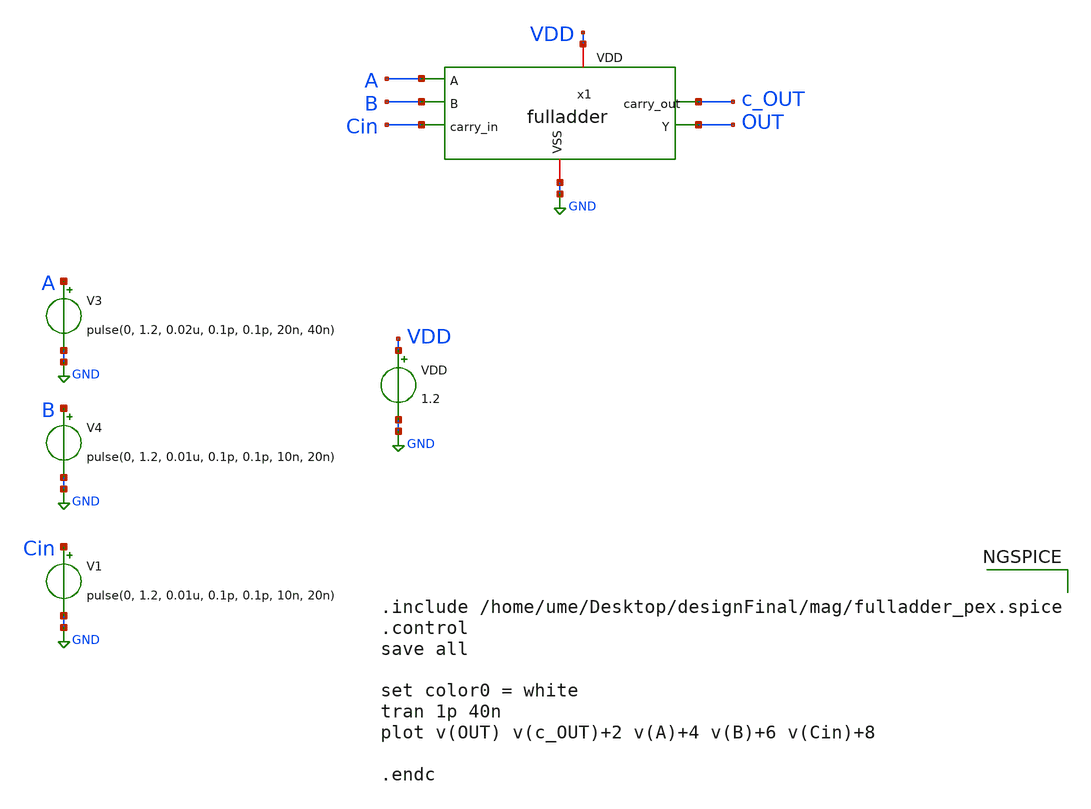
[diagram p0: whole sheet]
** sch_path: design/ALU/fulladder_tb.sch
**.subckt fulladder_tb
VDD VDD GND 1.2
V3 A GND pulse(0, 1.2, 0.02u, 0.1p, 0.1p, 20n, 40n)
V4 B GND pulse(0, 1.2, 0.01u, 0.1p, 0.1p, 10n, 20n)
V1 Cin GND pulse(0, 1.2, 0.01u, 0.1p, 0.1p, 10n, 20n)
x1 A B Cin VDD GND c_OUT OUT fulladder
**** begin user architecture code

** opencircuitdesign pdks install
.lib $::SKYWATER_MODELS/sky130.lib.spice tt_mm




.include /home/ume/Desktop/designFinal/mag/fulladder_pex.spice
.control
save all

set color0 = white
tran 1p 40n
plot v(OUT) v(c_OUT)+2 v(A)+4 v(B)+6 v(Cin)+8

.endc

**** end user architecture code
**.ends
.GLOBAL GND
.end
